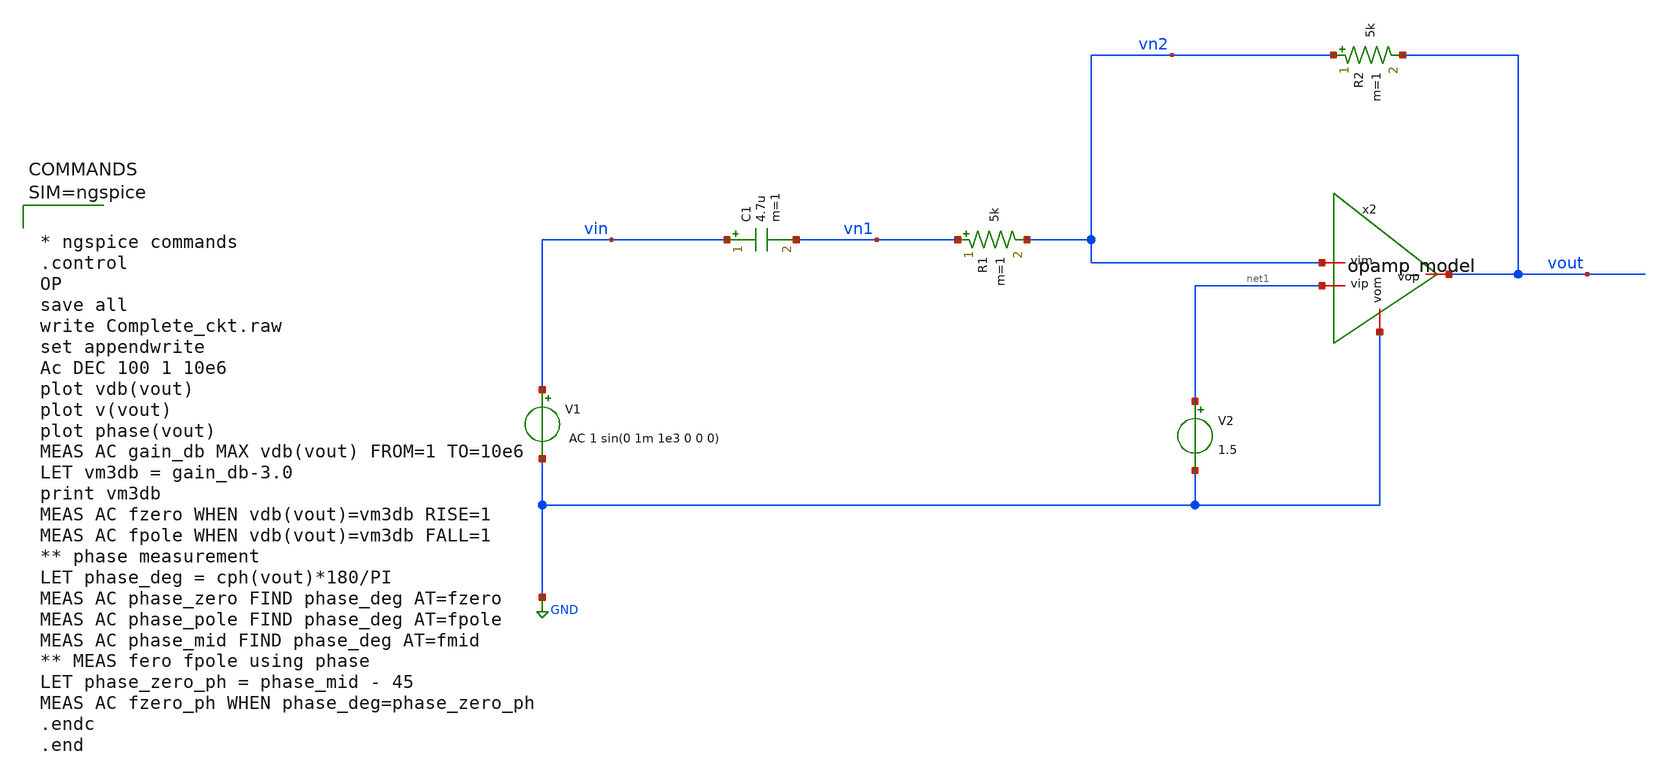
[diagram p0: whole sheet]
** sch_path: xschem/OP2.sch
**.subckt OP2
R1 vn1 vn2 5k m=1
R2 vn2 vout 5k m=1
C1 vin vn1 4.7u m=1
V1 vin GND AC 1 sin(0 1m 1e3 0 0 0)
V2 net1 GND 1.5
x2 vout net1 vn2 GND opamp_model
**** begin user architecture code



* ngspice commands
.control
OP
save all
write Complete_ckt.raw
set appendwrite
Ac DEC 100 1 10e6
plot vdb(vout)
plot v(vout)
plot phase(vout)
MEAS AC gain_db MAX vdb(vout) FROM=1 TO=10e6
LET vm3db = gain_db-3.0
print vm3db
MEAS AC fzero WHEN vdb(vout)=vm3db RISE=1
MEAS AC fpole WHEN vdb(vout)=vm3db FALL=1
** phase measurement
LET phase_deg = cph(vout)*180/PI
MEAS AC phase_zero FIND phase_deg AT=fzero
MEAS AC phase_pole FIND phase_deg AT=fpole
MEAS AC phase_mid FIND phase_deg AT=fmid
** MEAS fero fpole using phase
LET phase_zero_ph = phase_mid - 45
MEAS AC fzero_ph WHEN phase_deg=phase_zero_ph
.endc
.end



**** end user architecture code
**.ends

* expanding   symbol:  opamp_model.sym # of pins=4
** sym_path: xschem/opamp_model.sym
** sch_path: xschem/opamp_model.sch
.subckt opamp_model vop vip vim vom
*.iopin vop
*.iopin vom
*.iopin vip
*.iopin vim
E1 vop vom vip vim 1000
.ends

.GLOBAL GND
.end
